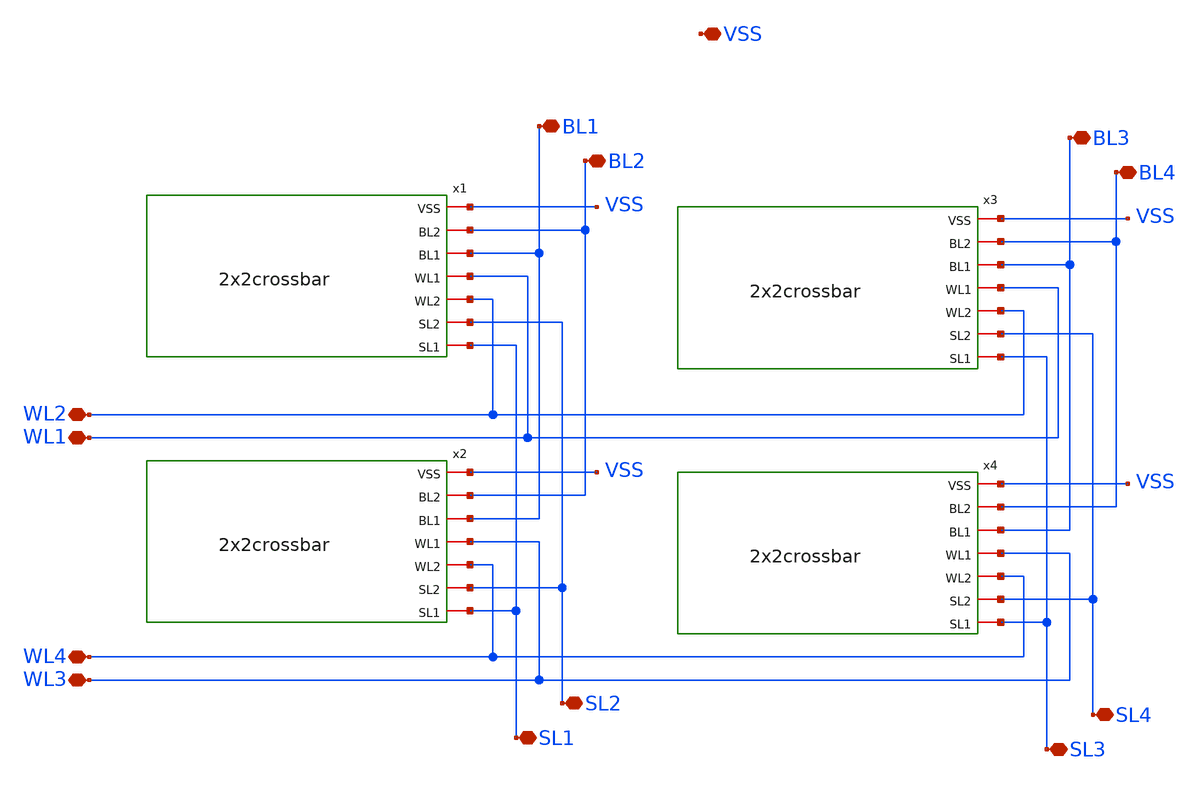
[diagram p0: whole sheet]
** sch_path: xschem/Crossbar/4x4crossbar.sch
* StefanSchippers/xschem_sky130/sky130_fd_pr/reram.sym:
* Copyright 2021 Stefan Frederik Schippers
* Licensed under the Apache License, Version 2.0 (the "License");
**.subckt 4x4crossbar BL1 BL2 SL2 SL1 BL3 BL4 SL4 SL3 WL2 WL1 WL4 WL3 VSS
*.iopin BL1
*.iopin BL2
*.iopin SL2
*.iopin SL1
*.iopin BL3
*.iopin BL4
*.iopin SL4
*.iopin SL3
*.iopin WL2
*.iopin WL1
*.iopin WL4
*.iopin WL3
*.iopin VSS
x1 VSS BL2 BL1 WL1 WL2 SL2 SL1 2x2crossbar
x2 VSS BL2 BL1 WL3 WL4 SL2 SL1 2x2crossbar
x3 VSS BL4 BL3 WL1 WL2 SL4 SL3 2x2crossbar
x4 VSS BL4 BL3 WL3 WL4 SL4 SL3 2x2crossbar
**.ends

* expanding   symbol:  Crossbar/2x2crossbar.sym # of pins=7
** sym_path: xschem/Crossbar/2x2crossbar.sym
** sch_path: xschem/Crossbar/2x2crossbar.sch
.subckt 2x2crossbar VSS BL2 BL1 WL1 WL2 SL2 SL1
*.iopin BL2
*.iopin BL1
*.iopin VSS
*.iopin WL1
*.iopin WL2
*.iopin SL1
*.iopin SL2
x1 BL1 WL1 VSS SL1 1T1R
x2 BL2 WL1 VSS SL2 1T1R
x3 BL1 WL2 VSS SL1 1T1R
x4 BL2 WL2 VSS SL2 1T1R
.ends


* expanding   symbol:  Crossbar/1T1R.sym # of pins=4
** sym_path: xschem/1T1R.sym
** sch_path: xschem/1T1R.sch
.subckt 1T1R BL WL VSS SL
*.iopin SL
*.iopin VSS
*.iopin WL
*.iopin BL
XR1 BL net1 sky130_fd_pr_reram__reram_cell Tfilament_0=3.8e-9
XM1 net1 WL SL VSS sky130_fd_pr__nfet_g5v0d10v5 L=0.5 W=7 nf=1 ad='int((nf+1)/2) * W/nf * 0.29' as='int((nf+2)/2) * W/nf * 0.29'
+ pd='2*int((nf+1)/2) * (W/nf + 0.29)' ps='2*int((nf+2)/2) * (W/nf + 0.29)' nrd='0.29 / W' nrs='0.29 / W'
+ sa=0 sb=0 sd=0 mult=1 m=1
.ends

**** begin user architecture code

.subckt sky130_fd_pr_reram__reram_cell TE BE Tfilament_0=3.3e-9 area_ox=0.1024e-12
N1 TE BE nFilament sky130_fd_pr_reram__reram_model
.ic v(nFilament)={Tfilament_0*1.0e9}
.ends sky130_fd_pr_reram__reram_cell

.model sky130_fd_pr_reram__reram_model sky130_fd_pr_reram__reram_module  area_ox = 0.1024e-12  Tox =
+ 5.0  Tfilament_max = 4.9  Tfilament_min = 3.3  Eact_generation = 1.501  Eact_recombination  = 1.500
+  I_k1  = 6.140e-5  Tfilament_ref = 4.7249  V_ref = 0.430  velocity_k1 = 150  gamma_k0  = 16.5  gamma_k1
+  = -1.25  Temperature_0 = 300  C_thermal = 3.1825e-16  tau_thermal = 0.23e-9  t_step  = 1.0e-9
+  smoothing = 1e-7  Kclip = 200

.control
pre_osdi $SKYWATER_MODELS/sky130_fd_pr_reram__reram_module.osdi
.endc

**** end user architecture code
.end
